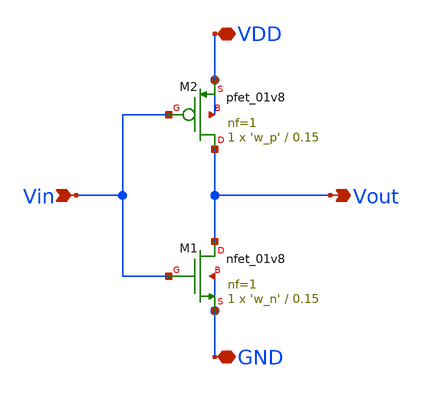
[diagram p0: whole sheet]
** sch_path: tt_um_emmersonv_tiq_adc/xschem/UNIT_INVERTER.sch
**.subckt UNIT_INVERTER Vout Vin VDD GND
*.opin Vout
*.ipin Vin
*.iopin VDD
*.iopin GND
XM1 Vout Vin GND GND sky130_fd_pr__nfet_01v8 L=0.15 W='w_n' nf=1 ad='int((nf+1)/2) * W/nf * 0.29' as='int((nf+2)/2) * W/nf * 0.29'
+ pd='2*int((nf+1)/2) * (W/nf + 0.29)' ps='2*int((nf+2)/2) * (W/nf + 0.29)' nrd='0.29 / W' nrs='0.29 / W'
+ sa=0 sb=0 sd=0 mult=1 m=1
XM2 Vout Vin VDD VDD sky130_fd_pr__pfet_01v8 L=0.15 W='w_p' nf=1 ad='int((nf+1)/2) * W/nf * 0.29' as='int((nf+2)/2) * W/nf * 0.29'
+ pd='2*int((nf+1)/2) * (W/nf + 0.29)' ps='2*int((nf+2)/2) * (W/nf + 0.29)' nrd='0.29 / W' nrs='0.29 / W'
+ sa=0 sb=0 sd=0 mult=1 m=1
**.ends
.end
